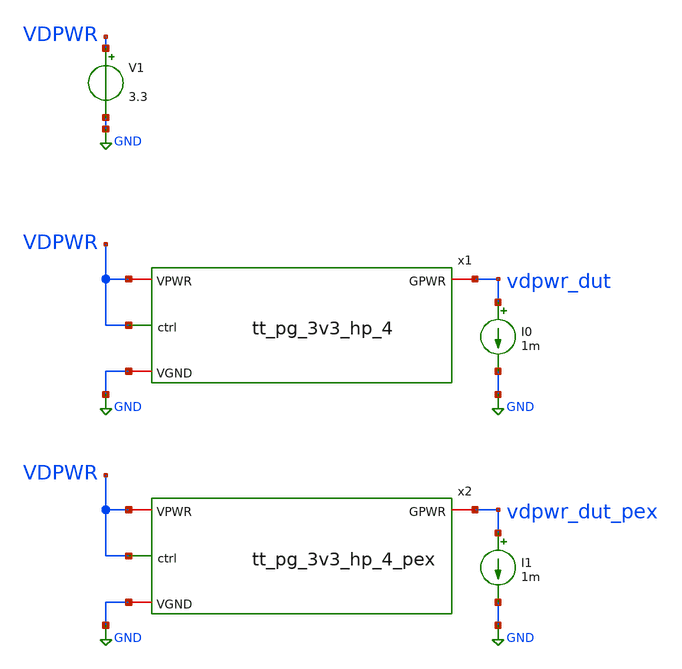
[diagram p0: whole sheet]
** sch_path: pg/gf180mcuD/tt_pg_3v3_hp_4/xschem/tb_rdson.sch
**.subckt tb_rdson
x1 GND VDPWR VDPWR vdpwr_dut tt_pg_3v3_hp_4
I0 vdpwr_dut GND 1m
V1 VDPWR GND 3.3
x2 GND VDPWR VDPWR vdpwr_dut_pex tt_pg_3v3_hp_4_pex
I1 vdpwr_dut_pex GND 1m
**** begin user architecture code

.include design.ngspice
.lib sm141064.ngspice typical



.control
save all
dc V1 2.7 3.6 0.05
plot ((v(vdpwr) - v(vdpwr_dut)) / 1m) ((v(vdpwr) - v(vdpwr_dut_pex)) / 1m)
write tb_rdson.raw
*quit 0
.endc
.end


**** end user architecture code
**.ends

* expanding   symbol:  tt_pg_3v3_hp_4.sym # of pins=4
** sym_path: pg/gf180mcuD/tt_pg_3v3_hp_4/xschem/tt_pg_3v3_hp_4.sym
** sch_path: pg/gf180mcuD/tt_pg_3v3_hp_4/xschem/tt_pg_3v3_hp_4.sch
.subckt tt_pg_3v3_hp_4 VGND VPWR ctrl GPWR
*.ipin ctrl
*.iopin VPWR
*.iopin VGND
*.iopin GPWR
x[1] VGND GPWR ctrl_n discharge_3v3
x[2] VGND GPWR ctrl_n discharge_3v3
XM1 ctrl_n ctrl VGND VGND nfet_03v3 L=0.28u W=11.0u nf=4 ad='int((nf+1)/2) * W/nf * 0.18u' as='int((nf+2)/2) * W/nf * 0.18u'
+ pd='2*int((nf+1)/2) * (W/nf + 0.18u)' ps='2*int((nf+2)/2) * (W/nf + 0.18u)' nrd='0.18u / W' nrs='0.18u / W'
+ sa=0 sb=0 sd=0 m=1 par=1
XM2 ctrl_n ctrl VPWR VPWR pfet_03v3 L=0.28u W=20.68u nf=4 ad='int((nf+1)/2) * W/nf * 0.18u' as='int((nf+2)/2) * W/nf * 0.18u'
+ pd='2*int((nf+1)/2) * (W/nf + 0.18u)' ps='2*int((nf+2)/2) * (W/nf + 0.18u)' nrd='0.18u / W' nrs='0.18u / W'
+ sa=0 sb=0 sd=0 m=1 par=1
XM3 GPWR ctrl_n VPWR VPWR pfet_03v3 L=0.28u W=7667u nf=902 ad='int((nf+1)/2) * W/nf * 0.18u' as='int((nf+2)/2) * W/nf * 0.18u'
+ pd='2*int((nf+1)/2) * (W/nf + 0.18u)' ps='2*int((nf+2)/2) * (W/nf + 0.18u)' nrd='0.18u / W' nrs='0.18u / W'
+ sa=0 sb=0 sd=0 m=1 par=1
.ends


* expanding   symbol:  tt_pg_3v3_hp_4_pex.sym # of pins=4
** sym_path: pg/gf180mcuD/tt_pg_3v3_hp_4/xschem/tt_pg_3v3_hp_4.sym
.include [file normalize ../mag/tt_pg_3v3_hp_4.pex.spice]

* expanding   symbol:  discharge_3v3.sym # of pins=3
** sym_path: pg/gf180mcuD/common/xschem/discharge_3v3.sym
** sch_path: pg/gf180mcuD/common/xschem/discharge_3v3.sch
.subckt discharge_3v3 VGND GPWR gate
*.iopin GPWR
*.iopin VGND
*.ipin gate
XM1 GPWR gate net3 VGND nfet_03v3 L=0.6u W=0.99u nf=1 ad='int((nf+1)/2) * W/nf * 0.18u' as='int((nf+2)/2) * W/nf * 0.18u'
+ pd='2*int((nf+1)/2) * (W/nf + 0.18u)' ps='2*int((nf+2)/2) * (W/nf + 0.18u)' nrd='0.18u / W' nrs='0.18u / W'
+ sa=0 sb=0 sd=0 m=1 par=1
XM2 net3 gate net2 VGND nfet_03v3 L=0.6u W=0.99u nf=1 ad='int((nf+1)/2) * W/nf * 0.18u' as='int((nf+2)/2) * W/nf * 0.18u'
+ pd='2*int((nf+1)/2) * (W/nf + 0.18u)' ps='2*int((nf+2)/2) * (W/nf + 0.18u)' nrd='0.18u / W' nrs='0.18u / W'
+ sa=0 sb=0 sd=0 m=1 par=1
XM3 net2 gate net1 VGND nfet_03v3 L=0.6u W=0.99u nf=1 ad='int((nf+1)/2) * W/nf * 0.18u' as='int((nf+2)/2) * W/nf * 0.18u'
+ pd='2*int((nf+1)/2) * (W/nf + 0.18u)' ps='2*int((nf+2)/2) * (W/nf + 0.18u)' nrd='0.18u / W' nrs='0.18u / W'
+ sa=0 sb=0 sd=0 m=1 par=1
XM4 net1 gate VGND VGND nfet_03v3 L=0.6u W=0.99u nf=1 ad='int((nf+1)/2) * W/nf * 0.18u' as='int((nf+2)/2) * W/nf * 0.18u'
+ pd='2*int((nf+1)/2) * (W/nf + 0.18u)' ps='2*int((nf+2)/2) * (W/nf + 0.18u)' nrd='0.18u / W' nrs='0.18u / W'
+ sa=0 sb=0 sd=0 m=1 par=1
XM5 GPWR gate net6 VGND nfet_03v3 L=0.6u W=0.99u nf=1 ad='int((nf+1)/2) * W/nf * 0.18u' as='int((nf+2)/2) * W/nf * 0.18u'
+ pd='2*int((nf+1)/2) * (W/nf + 0.18u)' ps='2*int((nf+2)/2) * (W/nf + 0.18u)' nrd='0.18u / W' nrs='0.18u / W'
+ sa=0 sb=0 sd=0 m=1 par=1
XM6 net6 gate net5 VGND nfet_03v3 L=0.6u W=0.99u nf=1 ad='int((nf+1)/2) * W/nf * 0.18u' as='int((nf+2)/2) * W/nf * 0.18u'
+ pd='2*int((nf+1)/2) * (W/nf + 0.18u)' ps='2*int((nf+2)/2) * (W/nf + 0.18u)' nrd='0.18u / W' nrs='0.18u / W'
+ sa=0 sb=0 sd=0 m=1 par=1
XM7 net5 gate net4 VGND nfet_03v3 L=0.6u W=0.99u nf=1 ad='int((nf+1)/2) * W/nf * 0.18u' as='int((nf+2)/2) * W/nf * 0.18u'
+ pd='2*int((nf+1)/2) * (W/nf + 0.18u)' ps='2*int((nf+2)/2) * (W/nf + 0.18u)' nrd='0.18u / W' nrs='0.18u / W'
+ sa=0 sb=0 sd=0 m=1 par=1
XM8 net4 gate VGND VGND nfet_03v3 L=0.6u W=0.99u nf=1 ad='int((nf+1)/2) * W/nf * 0.18u' as='int((nf+2)/2) * W/nf * 0.18u'
+ pd='2*int((nf+1)/2) * (W/nf + 0.18u)' ps='2*int((nf+2)/2) * (W/nf + 0.18u)' nrd='0.18u / W' nrs='0.18u / W'
+ sa=0 sb=0 sd=0 m=1 par=1
.ends

.GLOBAL GND
.end
